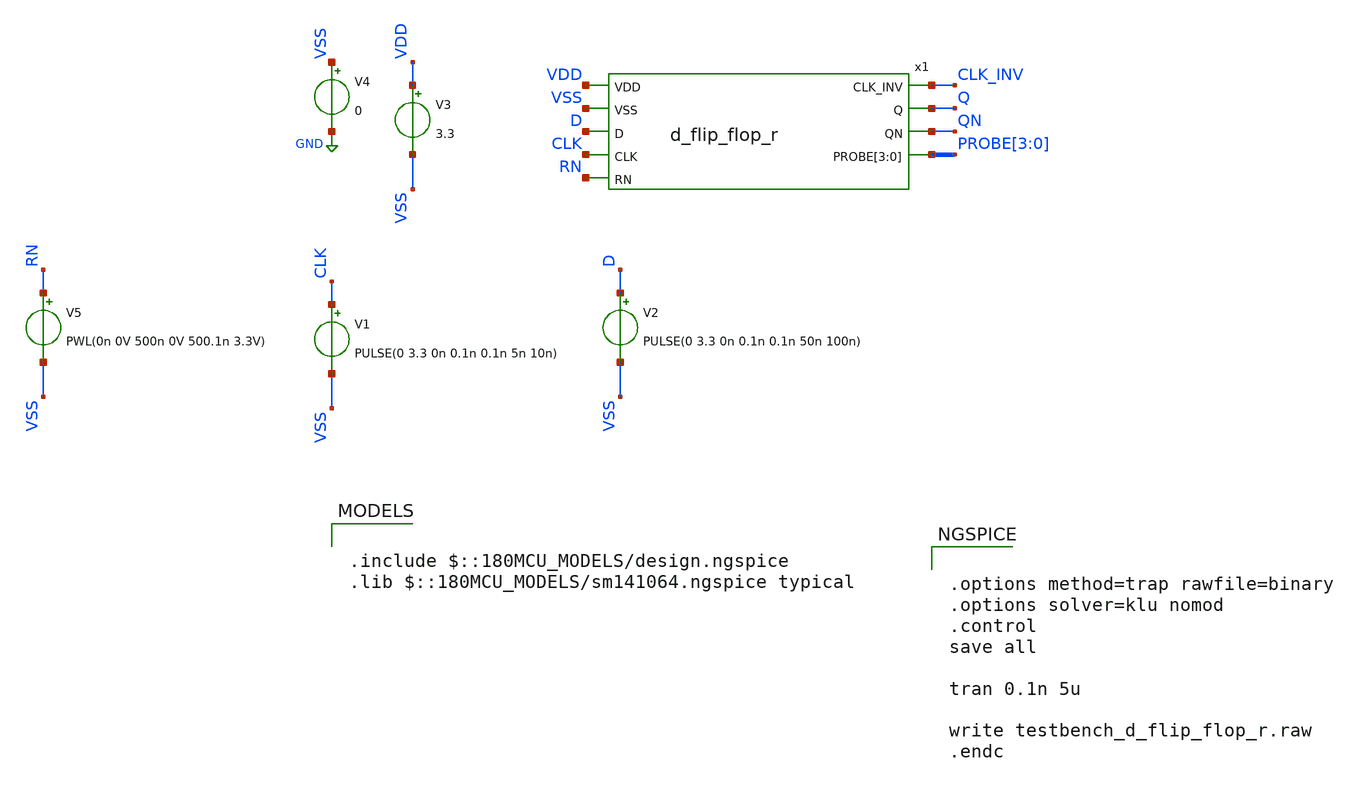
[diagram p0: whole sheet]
** sch_path: designs/libs/core_fpga/d_flip_flop/testbench_d_flip_flop_r.sch
**.subckt testbench_d_flip_flop_r
V1 CLK VSS PULSE(0 3.3 0n 0.1n 0.1n 5n 10n)
V2 D VSS PULSE(0 3.3 0n 0.1n 0.1n 50n 100n)
V3 VDD VSS 3.3
V4 VSS GND 0
V5 RN VSS PWL(0n 0V 500n 0V 500.1n 3.3V)
x1 VDD CLK_INV VSS Q D QN CLK PROBE[3] PROBE[2] PROBE[1] PROBE[0] RN d_flip_flop_r
**** begin user architecture code

.include $::180MCU_MODELS/design.ngspice
.lib $::180MCU_MODELS/sm141064.ngspice typical



.options method=trap rawfile=binary
.options solver=klu nomod
.control
save all

tran 0.1n 5u

write testbench_d_flip_flop_r.raw
.endc


**** end user architecture code
**.ends

* expanding   symbol:  sscs-chipathon2025-LNA/designs/libs/core_fpga/d_flip_flop/d_flip_flop_r.sym #
*+ of pins=9
** sym_path: sscs-chipathon2025-LNA/designs/libs/core_fpga/d_flip_flop/d_flip_flop_r.sym
** sch_path: sscs-chipathon2025-LNA/designs/libs/core_fpga/d_flip_flop/d_flip_flop_r.sch
.subckt d_flip_flop_r VDD CLK_INV VSS Q D QN CLK PROBE[3] PROBE[2] PROBE[1] PROBE[0] RN
*.ipin D
*.ipin VDD
*.ipin VSS
*.opin Q
*.ipin CLK
*.ipin RN
*.opin CLK_INV
*.opin QN
*.opin PROBE[3],PROBE[2],PROBE[1],PROBE[0]
XM1 net1 D VDD VDD pfet_03v3 L=0.3u W=1.7u nf=1 ad='int((nf+1)/2) * W/nf * 0.18u' as='int((nf+2)/2) * W/nf * 0.18u'
+ pd='2*int((nf+1)/2) * (W/nf + 0.18u)' ps='2*int((nf+2)/2) * (W/nf + 0.18u)' nrd='0.18u / W' nrs='0.18u / W'
+ sa=0 sb=0 sd=0 m=1
XM2 PROBE[0] CLK_INV net2 VSS nfet_03v3 L=0.3u W=0.85u nf=1 ad='int((nf+1)/2) * W/nf * 0.18u' as='int((nf+2)/2) * W/nf * 0.18u'
+ pd='2*int((nf+1)/2) * (W/nf + 0.18u)' ps='2*int((nf+2)/2) * (W/nf + 0.18u)' nrd='0.18u / W' nrs='0.18u / W'
+ sa=0 sb=0 sd=0 m=1
XM3 PROBE[0] CLK net1 VDD pfet_03v3 L=0.3u W=1.7u nf=1 ad='int((nf+1)/2) * W/nf * 0.18u' as='int((nf+2)/2) * W/nf * 0.18u'
+ pd='2*int((nf+1)/2) * (W/nf + 0.18u)' ps='2*int((nf+2)/2) * (W/nf + 0.18u)' nrd='0.18u / W' nrs='0.18u / W'
+ sa=0 sb=0 sd=0 m=1
XM4 net2 D VSS VSS nfet_03v3 L=0.3u W=0.85u nf=1 ad='int((nf+1)/2) * W/nf * 0.18u' as='int((nf+2)/2) * W/nf * 0.18u'
+ pd='2*int((nf+1)/2) * (W/nf + 0.18u)' ps='2*int((nf+2)/2) * (W/nf + 0.18u)' nrd='0.18u / W' nrs='0.18u / W'
+ sa=0 sb=0 sd=0 m=1
XM5 CLK_INV CLK VDD VDD pfet_03v3 L=0.3u W=1.7u nf=1 ad='int((nf+1)/2) * W/nf * 0.18u' as='int((nf+2)/2) * W/nf * 0.18u'
+ pd='2*int((nf+1)/2) * (W/nf + 0.18u)' ps='2*int((nf+2)/2) * (W/nf + 0.18u)' nrd='0.18u / W' nrs='0.18u / W'
+ sa=0 sb=0 sd=0 m=1
XM8 CLK_INV CLK VSS VSS nfet_03v3 L=0.3u W=0.85u nf=1 ad='int((nf+1)/2) * W/nf * 0.18u' as='int((nf+2)/2) * W/nf * 0.18u'
+ pd='2*int((nf+1)/2) * (W/nf + 0.18u)' ps='2*int((nf+2)/2) * (W/nf + 0.18u)' nrd='0.18u / W' nrs='0.18u / W'
+ sa=0 sb=0 sd=0 m=1
XM13 net3 PROBE[1] VDD VDD pfet_03v3 L=0.3u W=1.7u nf=1 ad='int((nf+1)/2) * W/nf * 0.18u' as='int((nf+2)/2) * W/nf * 0.18u'
+ pd='2*int((nf+1)/2) * (W/nf + 0.18u)' ps='2*int((nf+2)/2) * (W/nf + 0.18u)' nrd='0.18u / W' nrs='0.18u / W'
+ sa=0 sb=0 sd=0 m=1
XM14 PROBE[0] CLK net4 VSS nfet_03v3 L=0.3u W=0.85u nf=1 ad='int((nf+1)/2) * W/nf * 0.18u' as='int((nf+2)/2) * W/nf * 0.18u'
+ pd='2*int((nf+1)/2) * (W/nf + 0.18u)' ps='2*int((nf+2)/2) * (W/nf + 0.18u)' nrd='0.18u / W' nrs='0.18u / W'
+ sa=0 sb=0 sd=0 m=1
XM15 PROBE[0] CLK_INV net3 VDD pfet_03v3 L=0.3u W=1.7u nf=1 ad='int((nf+1)/2) * W/nf * 0.18u' as='int((nf+2)/2) * W/nf * 0.18u'
+ pd='2*int((nf+1)/2) * (W/nf + 0.18u)' ps='2*int((nf+2)/2) * (W/nf + 0.18u)' nrd='0.18u / W' nrs='0.18u / W'
+ sa=0 sb=0 sd=0 m=1
XM16 net4 PROBE[1] VSS VSS nfet_03v3 L=0.3u W=0.85u nf=1 ad='int((nf+1)/2) * W/nf * 0.18u' as='int((nf+2)/2) * W/nf * 0.18u'
+ pd='2*int((nf+1)/2) * (W/nf + 0.18u)' ps='2*int((nf+2)/2) * (W/nf + 0.18u)' nrd='0.18u / W' nrs='0.18u / W'
+ sa=0 sb=0 sd=0 m=1
XM9 net5 PROBE[1] VDD VDD pfet_03v3 L=0.3u W=1.7u nf=1 ad='int((nf+1)/2) * W/nf * 0.18u' as='int((nf+2)/2) * W/nf * 0.18u'
+ pd='2*int((nf+1)/2) * (W/nf + 0.18u)' ps='2*int((nf+2)/2) * (W/nf + 0.18u)' nrd='0.18u / W' nrs='0.18u / W'
+ sa=0 sb=0 sd=0 m=1
XM10 PROBE[2] CLK net6 VSS nfet_03v3 L=0.3u W=0.85u nf=1 ad='int((nf+1)/2) * W/nf * 0.18u' as='int((nf+2)/2) * W/nf * 0.18u'
+ pd='2*int((nf+1)/2) * (W/nf + 0.18u)' ps='2*int((nf+2)/2) * (W/nf + 0.18u)' nrd='0.18u / W' nrs='0.18u / W'
+ sa=0 sb=0 sd=0 m=1
XM11 PROBE[2] CLK_INV net5 VDD pfet_03v3 L=0.3u W=1.7u nf=1 ad='int((nf+1)/2) * W/nf * 0.18u' as='int((nf+2)/2) * W/nf * 0.18u'
+ pd='2*int((nf+1)/2) * (W/nf + 0.18u)' ps='2*int((nf+2)/2) * (W/nf + 0.18u)' nrd='0.18u / W' nrs='0.18u / W'
+ sa=0 sb=0 sd=0 m=1
XM12 net6 PROBE[1] VSS VSS nfet_03v3 L=0.3u W=0.85u nf=1 ad='int((nf+1)/2) * W/nf * 0.18u' as='int((nf+2)/2) * W/nf * 0.18u'
+ pd='2*int((nf+1)/2) * (W/nf + 0.18u)' ps='2*int((nf+2)/2) * (W/nf + 0.18u)' nrd='0.18u / W' nrs='0.18u / W'
+ sa=0 sb=0 sd=0 m=1
XM19 net7 PROBE[3] VDD VDD pfet_03v3 L=0.3u W=1.7u nf=1 ad='int((nf+1)/2) * W/nf * 0.18u' as='int((nf+2)/2) * W/nf * 0.18u'
+ pd='2*int((nf+1)/2) * (W/nf + 0.18u)' ps='2*int((nf+2)/2) * (W/nf + 0.18u)' nrd='0.18u / W' nrs='0.18u / W'
+ sa=0 sb=0 sd=0 m=1
XM20 PROBE[2] CLK_INV net8 VSS nfet_03v3 L=0.3u W=0.85u nf=1 ad='int((nf+1)/2) * W/nf * 0.18u' as='int((nf+2)/2) * W/nf * 0.18u'
+ pd='2*int((nf+1)/2) * (W/nf + 0.18u)' ps='2*int((nf+2)/2) * (W/nf + 0.18u)' nrd='0.18u / W' nrs='0.18u / W'
+ sa=0 sb=0 sd=0 m=1
XM21 PROBE[2] CLK net7 VDD pfet_03v3 L=0.3u W=1.7u nf=1 ad='int((nf+1)/2) * W/nf * 0.18u' as='int((nf+2)/2) * W/nf * 0.18u'
+ pd='2*int((nf+1)/2) * (W/nf + 0.18u)' ps='2*int((nf+2)/2) * (W/nf + 0.18u)' nrd='0.18u / W' nrs='0.18u / W'
+ sa=0 sb=0 sd=0 m=1
XM22 net8 PROBE[3] VSS VSS nfet_03v3 L=0.3u W=0.85u nf=1 ad='int((nf+1)/2) * W/nf * 0.18u' as='int((nf+2)/2) * W/nf * 0.18u'
+ pd='2*int((nf+1)/2) * (W/nf + 0.18u)' ps='2*int((nf+2)/2) * (W/nf + 0.18u)' nrd='0.18u / W' nrs='0.18u / W'
+ sa=0 sb=0 sd=0 m=1
XM23 QN PROBE[3] VDD VDD pfet_03v3 L=0.3u W=1.7u nf=1 ad='int((nf+1)/2) * W/nf * 0.18u' as='int((nf+2)/2) * W/nf * 0.18u'
+ pd='2*int((nf+1)/2) * (W/nf + 0.18u)' ps='2*int((nf+2)/2) * (W/nf + 0.18u)' nrd='0.18u / W' nrs='0.18u / W'
+ sa=0 sb=0 sd=0 m=1
XM24 QN PROBE[3] VSS VSS nfet_03v3 L=0.3u W=0.85u nf=1 ad='int((nf+1)/2) * W/nf * 0.18u' as='int((nf+2)/2) * W/nf * 0.18u'
+ pd='2*int((nf+1)/2) * (W/nf + 0.18u)' ps='2*int((nf+2)/2) * (W/nf + 0.18u)' nrd='0.18u / W' nrs='0.18u / W'
+ sa=0 sb=0 sd=0 m=1
XM25 Q QN VDD VDD pfet_03v3 L=0.3u W=1.7u nf=1 ad='int((nf+1)/2) * W/nf * 0.18u' as='int((nf+2)/2) * W/nf * 0.18u'
+ pd='2*int((nf+1)/2) * (W/nf + 0.18u)' ps='2*int((nf+2)/2) * (W/nf + 0.18u)' nrd='0.18u / W' nrs='0.18u / W'
+ sa=0 sb=0 sd=0 m=1
XM26 Q QN VSS VSS nfet_03v3 L=0.3u W=0.85u nf=1 ad='int((nf+1)/2) * W/nf * 0.18u' as='int((nf+2)/2) * W/nf * 0.18u'
+ pd='2*int((nf+1)/2) * (W/nf + 0.18u)' ps='2*int((nf+2)/2) * (W/nf + 0.18u)' nrd='0.18u / W' nrs='0.18u / W'
+ sa=0 sb=0 sd=0 m=1
XM6 net9 PROBE[0] VDD VDD pfet_03v3 L=0.3u W=1.7u nf=1 ad='int((nf+1)/2) * W/nf * 0.18u' as='int((nf+2)/2) * W/nf * 0.18u'
+ pd='2*int((nf+1)/2) * (W/nf + 0.18u)' ps='2*int((nf+2)/2) * (W/nf + 0.18u)' nrd='0.18u / W' nrs='0.18u / W'
+ sa=0 sb=0 sd=0 m=1
XM27 PROBE[1] RN net9 VDD pfet_03v3 L=0.3u W=1.7u nf=1 ad='int((nf+1)/2) * W/nf * 0.18u' as='int((nf+2)/2) * W/nf * 0.18u'
+ pd='2*int((nf+1)/2) * (W/nf + 0.18u)' ps='2*int((nf+2)/2) * (W/nf + 0.18u)' nrd='0.18u / W' nrs='0.18u / W'
+ sa=0 sb=0 sd=0 m=1
XM28 PROBE[1] PROBE[0] VSS VSS nfet_03v3 L=0.3u W=0.85u nf=1 ad='int((nf+1)/2) * W/nf * 0.18u' as='int((nf+2)/2) * W/nf * 0.18u'
+ pd='2*int((nf+1)/2) * (W/nf + 0.18u)' ps='2*int((nf+2)/2) * (W/nf + 0.18u)' nrd='0.18u / W' nrs='0.18u / W'
+ sa=0 sb=0 sd=0 m=1
XM17 net10 PROBE[2] VDD VDD pfet_03v3 L=0.3u W=1.7u nf=1 ad='int((nf+1)/2) * W/nf * 0.18u' as='int((nf+2)/2) * W/nf * 0.18u'
+ pd='2*int((nf+1)/2) * (W/nf + 0.18u)' ps='2*int((nf+2)/2) * (W/nf + 0.18u)' nrd='0.18u / W' nrs='0.18u / W'
+ sa=0 sb=0 sd=0 m=1
XM29 PROBE[3] RN net10 VDD pfet_03v3 L=0.3u W=1.7u nf=1 ad='int((nf+1)/2) * W/nf * 0.18u' as='int((nf+2)/2) * W/nf * 0.18u'
+ pd='2*int((nf+1)/2) * (W/nf + 0.18u)' ps='2*int((nf+2)/2) * (W/nf + 0.18u)' nrd='0.18u / W' nrs='0.18u / W'
+ sa=0 sb=0 sd=0 m=1
XM30 PROBE[3] PROBE[2] VSS VSS nfet_03v3 L=0.3u W=0.85u nf=1 ad='int((nf+1)/2) * W/nf * 0.18u' as='int((nf+2)/2) * W/nf * 0.18u'
+ pd='2*int((nf+1)/2) * (W/nf + 0.18u)' ps='2*int((nf+2)/2) * (W/nf + 0.18u)' nrd='0.18u / W' nrs='0.18u / W'
+ sa=0 sb=0 sd=0 m=1
XM7 PROBE[1] RN VSS VSS nfet_03v3 L=0.3u W=0.85u nf=1 ad='int((nf+1)/2) * W/nf * 0.18u' as='int((nf+2)/2) * W/nf * 0.18u'
+ pd='2*int((nf+1)/2) * (W/nf + 0.18u)' ps='2*int((nf+2)/2) * (W/nf + 0.18u)' nrd='0.18u / W' nrs='0.18u / W'
+ sa=0 sb=0 sd=0 m=1
XM18 PROBE[3] RN VSS VSS nfet_03v3 L=0.3u W=0.85u nf=1 ad='int((nf+1)/2) * W/nf * 0.18u' as='int((nf+2)/2) * W/nf * 0.18u'
+ pd='2*int((nf+1)/2) * (W/nf + 0.18u)' ps='2*int((nf+2)/2) * (W/nf + 0.18u)' nrd='0.18u / W' nrs='0.18u / W'
+ sa=0 sb=0 sd=0 m=1
.ends

.GLOBAL GND
.end
